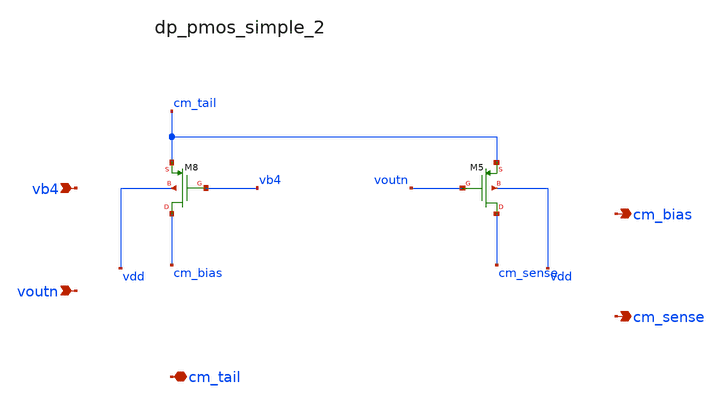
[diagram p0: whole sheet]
** sch_path: analog-db/raw/amp_027_fan_rrl_ota/hier/blocks/dp_pmos_simple_2.sch
**.subckt dp_pmos_simple_2 vb4 voutn cm_tail cm_bias cm_sense
*.ipin vb4
*.ipin voutn
*.iopin cm_tail
*.opin cm_bias
*.opin cm_sense
XM5 cm_sense voutn cm_tail vdd sg13_lv_pmos w=x_dut_xm5_w l=x_dut_xm5_l ng=1 m=x_dut_xm5_m
XM8 cm_bias vb4 cm_tail vdd sg13_lv_pmos w=x_dut_xm8_w l=x_dut_xm8_l ng=1 m=x_dut_xm8_m
**.ends
.end
